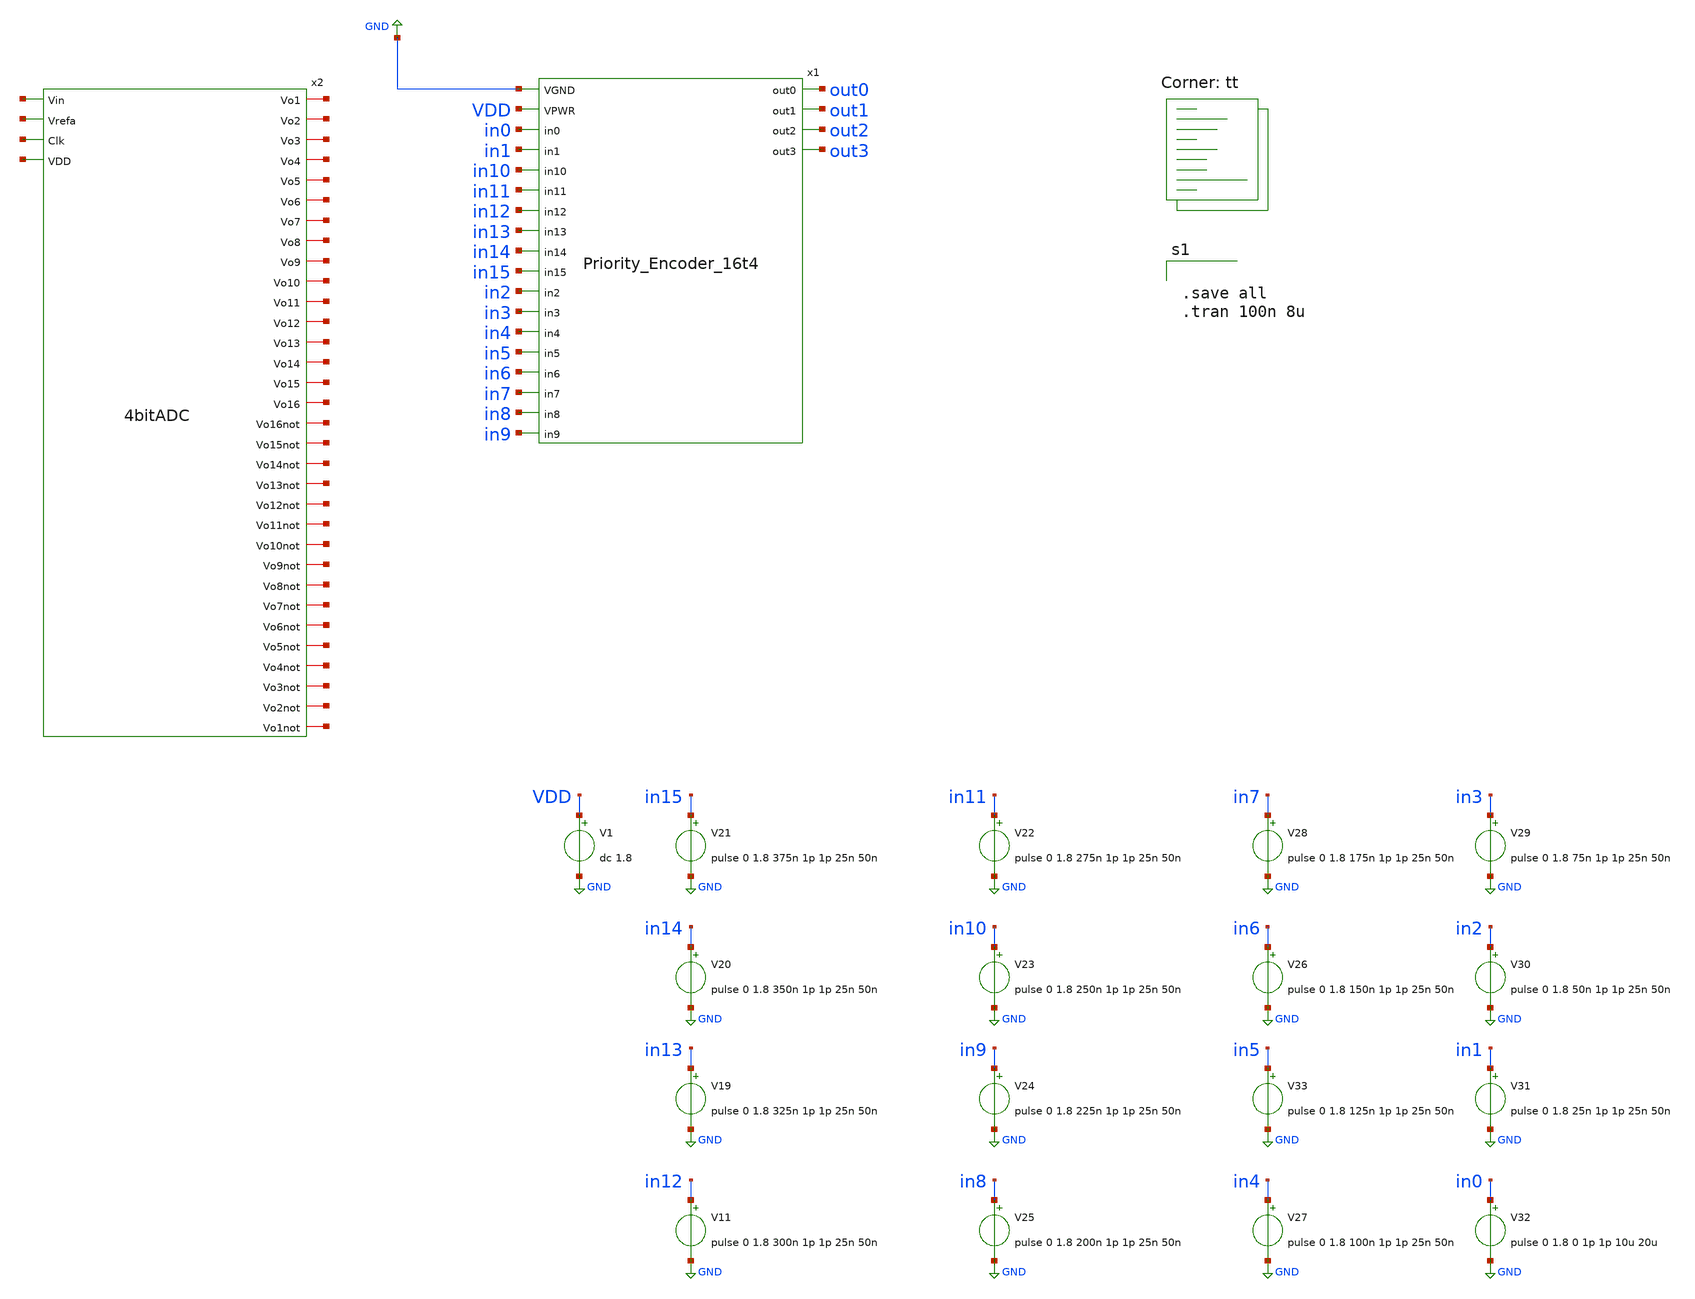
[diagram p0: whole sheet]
** sch_path: userLib/userLib/P_Encoder_Test.sch
**.subckt P_Encoder_Test
V1 VDD GND dc 1.8
x1 GND VDD in0 in1 in10 in11 in12 in13 in14 in15 in2 in3 in4 in5 in6 in7 in8 in9 out0 out1 out2 out3
+ Priority_Encoder_16t4
V11 in12 GND pulse 0 1.8 300n 1p 1p 25n 50n
V19 in13 GND pulse 0 1.8 325n 1p 1p 25n 50n
V20 in14 GND pulse 0 1.8 350n 1p 1p 25n 50n
V21 in15 GND pulse 0 1.8 375n 1p 1p 25n 50n
V22 in11 GND pulse 0 1.8 275n 1p 1p 25n 50n
V23 in10 GND pulse 0 1.8 250n 1p 1p 25n 50n
V24 in9 GND pulse 0 1.8 225n 1p 1p 25n 50n
V25 in8 GND pulse 0 1.8 200n 1p 1p 25n 50n
V26 in6 GND pulse 0 1.8 150n 1p 1p 25n 50n
V27 in4 GND pulse 0 1.8 100n 1p 1p 25n 50n
V28 in7 GND pulse 0 1.8 175n 1p 1p 25n 50n
V29 in3 GND pulse 0 1.8 75n 1p 1p 25n 50n
V30 in2 GND pulse 0 1.8 50n 1p 1p 25n 50n
V31 in1 GND pulse 0 1.8 25n 1p 1p 25n 50n
V32 in0 GND pulse 0 1.8 0 1p 1p 10u 20u
V33 in5 GND pulse 0 1.8 125n 1p 1p 25n 50n
x2 net1 net2 net3 net4 net5 net6 net7 net8 net9 net10 net11 net12 net13 net14 net15 net16 net17
+ net18 net19 net20 net21 net22 net23 net24 net25 net26 net27 net28 net29 net30 net31 net32 net33 net34
+ net35 net36 4bitADC
**** begin user architecture code
.lib $::SKYWATER_MODELS/sky130.lib.spice tt


.save all
.tran 100n 8u



** opencircuitdesign pdks install
.include $::SKYWATER_STDCELLS/sky130_fd_sc_hd.spice


**** end user architecture code
**.ends
.GLOBAL GND
.end
